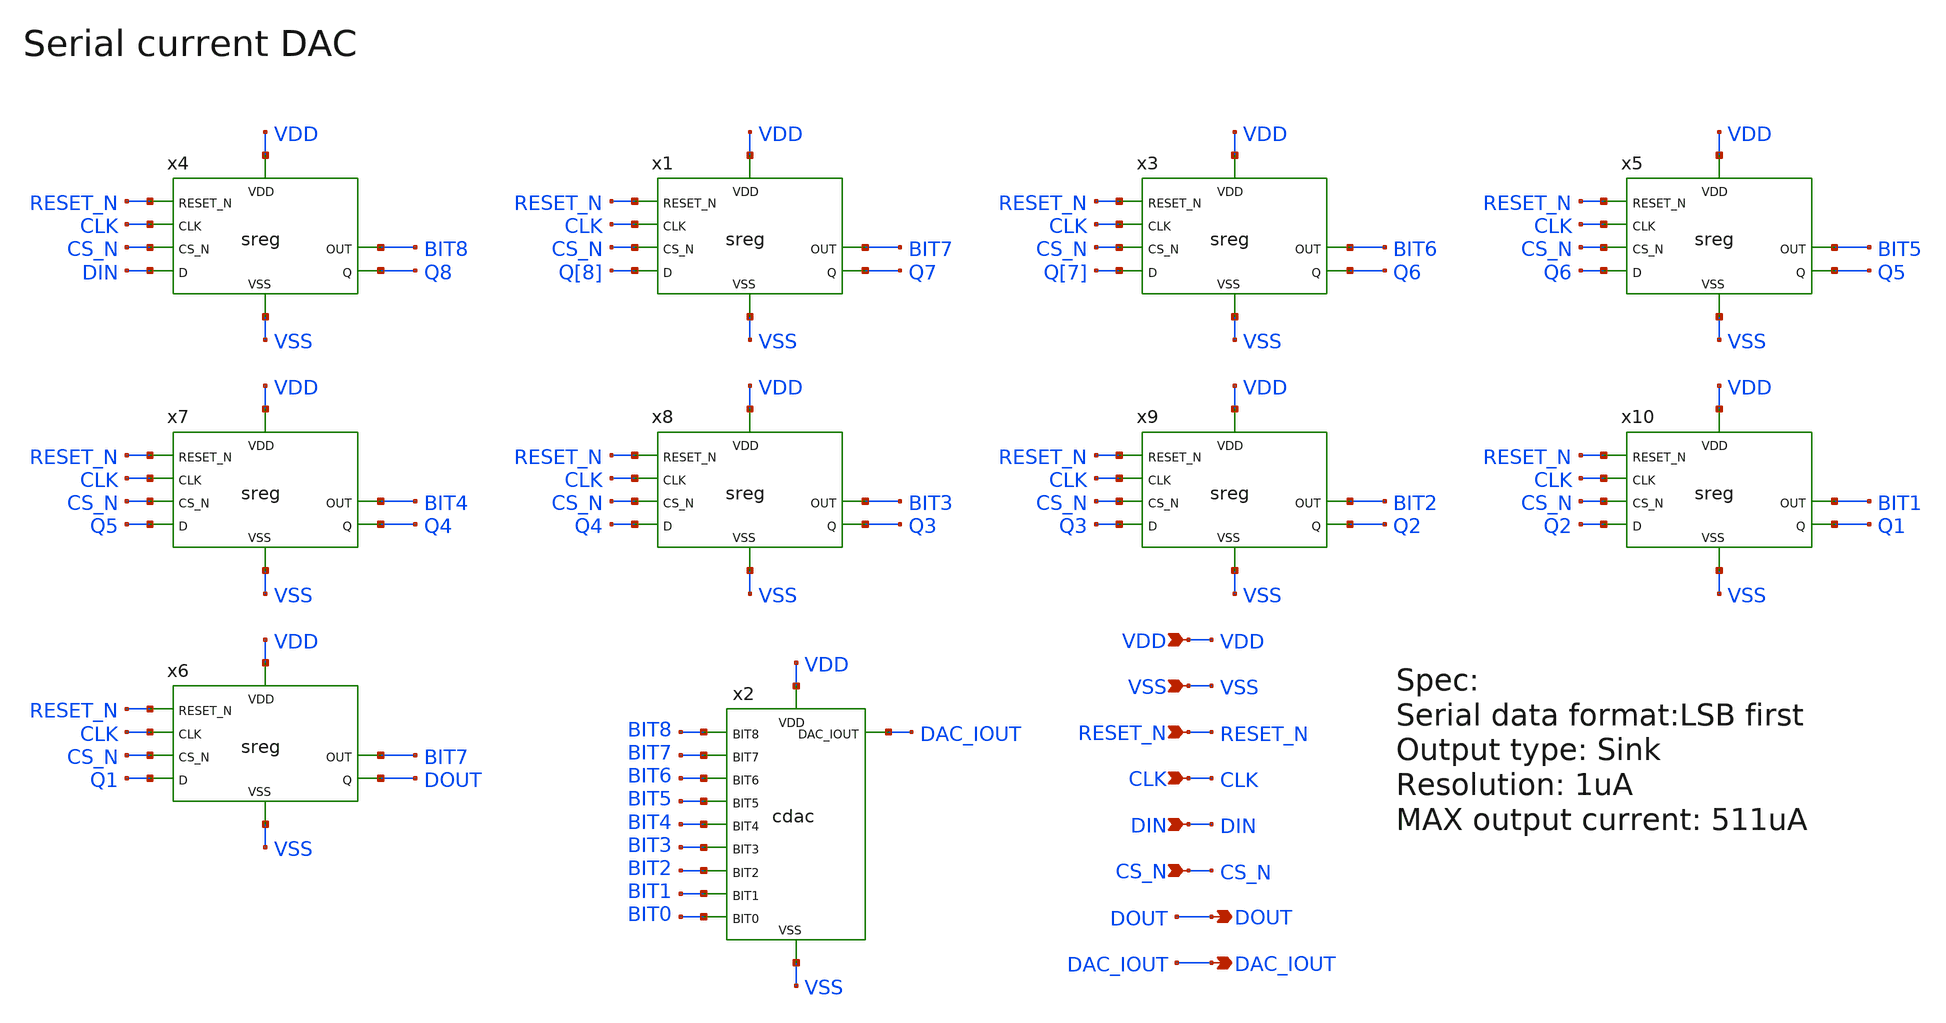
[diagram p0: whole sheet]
** sch_path: designs/libs/core_analog/scdac/scdac.sch
* Copyright 2022 GlobalFoundries PDK Authors
* Licensed under the Apache License, Version 2.0 (the "License");
* you may not use this file except in compliance with the License.
* You may obtain a copy of the License at
* https://www.apache.org/licenses/LICENSE-2.0
* Unless required by applicable law or agreed to in writing, software
* distributed under the License is distributed on an "AS IS" BASIS,
* WITHOUT WARRANTIES OR CONDITIONS OF ANY KIND, either express or implied.
* See the License for the specific language governing permissions and
* limitations under the License.
**.subckt scdac DAC_IOUT RESET_N CLK DIN CS_N VSS VDD DOUT
*.opin DAC_IOUT
*.ipin RESET_N
*.ipin CLK
*.ipin DIN
*.ipin CS_N
*.ipin VSS
*.ipin VDD
*.opin DOUT
x2 DAC_IOUT VSS VDD BIT8 BIT7 BIT6 BIT5 BIT4 BIT3 BIT2 BIT1 BIT0 cdac
x4 VDD VSS RESET_N CLK DIN CS_N Q8 BIT8 sreg
x1 VDD VSS RESET_N CLK Q[8] CS_N Q7 BIT7 sreg
x3 VDD VSS RESET_N CLK Q[7] CS_N Q6 BIT6 sreg
x5 VDD VSS RESET_N CLK Q6 CS_N Q5 BIT5 sreg
x6 VDD VSS RESET_N CLK Q1 CS_N DOUT BIT7 sreg
x7 VDD VSS RESET_N CLK Q5 CS_N Q4 BIT4 sreg
x8 VDD VSS RESET_N CLK Q4 CS_N Q3 BIT3 sreg
x9 VDD VSS RESET_N CLK Q3 CS_N Q2 BIT2 sreg
x10 VDD VSS RESET_N CLK Q2 CS_N Q1 BIT1 sreg
**.ends

* expanding   symbol:  libs/core_analog/scdac/cdac.sym # of pins=12
** sym_path: designs/libs/core_analog/scdac/cdac.sym
** sch_path: designs/libs/core_analog/scdac/cdac.sch
.subckt cdac DAC_IOUT VSS VDD BIT8 BIT7 BIT6 BIT5 BIT4 BIT3 BIT2 BIT1 BIT0
*.ipin BIT8
*.ipin BIT7
*.ipin BIT6
*.ipin BIT5
*.ipin BIT4
*.ipin BIT3
*.ipin BIT2
*.ipin BIT1
*.ipin BIT0
*.ipin VDD
*.ipin VSS
*.opin DAC_IOUT
XM8 64uA_REF 64uA_REF VSS VSS nfet_03v3 L=1u W=64u nf=1 ad='int((nf+1)/2) * W/nf * 0.18u' as='int((nf+2)/2) * W/nf * 0.18u'
+ pd='2*int((nf+1)/2) * (W/nf + 0.18u)' ps='2*int((nf+2)/2) * (W/nf + 0.18u)' nrd='0.18u / W' nrs='0.18u / W'
+ sa=0 sb=0 sd=0 m=1
XM11 net1 64uA_REF VSS VSS nfet_03v3 L=1u W=61.1u nf=1 ad='int((nf+1)/2) * W/nf * 0.18u' as='int((nf+2)/2) * W/nf * 0.18u'
+ pd='2*int((nf+1)/2) * (W/nf + 0.18u)' ps='2*int((nf+2)/2) * (W/nf + 0.18u)' nrd='0.18u / W' nrs='0.18u / W'
+ sa=0 sb=0 sd=0 m=1
XM13 DAC_IOUT BIT8 net1 VSS nfet_03v3 L=0.28u W=4u nf=1 ad='int((nf+1)/2) * W/nf * 0.18u' as='int((nf+2)/2) * W/nf * 0.18u'
+ pd='2*int((nf+1)/2) * (W/nf + 0.18u)' ps='2*int((nf+2)/2) * (W/nf + 0.18u)' nrd='0.18u / W' nrs='0.18u / W'
+ sa=0 sb=0 sd=0 m=1
XM15 net2 64uA_REF VSS VSS nfet_03v3 L=1u W=61.1u nf=1 ad='int((nf+1)/2) * W/nf * 0.18u' as='int((nf+2)/2) * W/nf * 0.18u'
+ pd='2*int((nf+1)/2) * (W/nf + 0.18u)' ps='2*int((nf+2)/2) * (W/nf + 0.18u)' nrd='0.18u / W' nrs='0.18u / W'
+ sa=0 sb=0 sd=0 m=1
XM16 DAC_IOUT BIT8 net2 VSS nfet_03v3 L=0.28u W=4u nf=1 ad='int((nf+1)/2) * W/nf * 0.18u' as='int((nf+2)/2) * W/nf * 0.18u'
+ pd='2*int((nf+1)/2) * (W/nf + 0.18u)' ps='2*int((nf+2)/2) * (W/nf + 0.18u)' nrd='0.18u / W' nrs='0.18u / W'
+ sa=0 sb=0 sd=0 m=1
XM18 net3 64uA_REF VSS VSS nfet_03v3 L=1u W=61.1u nf=1 ad='int((nf+1)/2) * W/nf * 0.18u' as='int((nf+2)/2) * W/nf * 0.18u'
+ pd='2*int((nf+1)/2) * (W/nf + 0.18u)' ps='2*int((nf+2)/2) * (W/nf + 0.18u)' nrd='0.18u / W' nrs='0.18u / W'
+ sa=0 sb=0 sd=0 m=1
XM19 DAC_IOUT BIT8 net3 VSS nfet_03v3 L=0.28u W=4u nf=1 ad='int((nf+1)/2) * W/nf * 0.18u' as='int((nf+2)/2) * W/nf * 0.18u'
+ pd='2*int((nf+1)/2) * (W/nf + 0.18u)' ps='2*int((nf+2)/2) * (W/nf + 0.18u)' nrd='0.18u / W' nrs='0.18u / W'
+ sa=0 sb=0 sd=0 m=1
XM21 net4 64uA_REF VSS VSS nfet_03v3 L=1u W=61.1u nf=1 ad='int((nf+1)/2) * W/nf * 0.18u' as='int((nf+2)/2) * W/nf * 0.18u'
+ pd='2*int((nf+1)/2) * (W/nf + 0.18u)' ps='2*int((nf+2)/2) * (W/nf + 0.18u)' nrd='0.18u / W' nrs='0.18u / W'
+ sa=0 sb=0 sd=0 m=1
XM22 DAC_IOUT BIT8 net4 VSS nfet_03v3 L=0.28u W=4u nf=1 ad='int((nf+1)/2) * W/nf * 0.18u' as='int((nf+2)/2) * W/nf * 0.18u'
+ pd='2*int((nf+1)/2) * (W/nf + 0.18u)' ps='2*int((nf+2)/2) * (W/nf + 0.18u)' nrd='0.18u / W' nrs='0.18u / W'
+ sa=0 sb=0 sd=0 m=1
XM24 net5 64uA_REF VSS VSS nfet_03v3 L=1u W=61.1u nf=1 ad='int((nf+1)/2) * W/nf * 0.18u' as='int((nf+2)/2) * W/nf * 0.18u'
+ pd='2*int((nf+1)/2) * (W/nf + 0.18u)' ps='2*int((nf+2)/2) * (W/nf + 0.18u)' nrd='0.18u / W' nrs='0.18u / W'
+ sa=0 sb=0 sd=0 m=1
XM25 DAC_IOUT BIT7 net5 VSS nfet_03v3 L=0.28u W=4u nf=1 ad='int((nf+1)/2) * W/nf * 0.18u' as='int((nf+2)/2) * W/nf * 0.18u'
+ pd='2*int((nf+1)/2) * (W/nf + 0.18u)' ps='2*int((nf+2)/2) * (W/nf + 0.18u)' nrd='0.18u / W' nrs='0.18u / W'
+ sa=0 sb=0 sd=0 m=1
XM27 net6 64uA_REF VSS VSS nfet_03v3 L=1u W=61.1u nf=1 ad='int((nf+1)/2) * W/nf * 0.18u' as='int((nf+2)/2) * W/nf * 0.18u'
+ pd='2*int((nf+1)/2) * (W/nf + 0.18u)' ps='2*int((nf+2)/2) * (W/nf + 0.18u)' nrd='0.18u / W' nrs='0.18u / W'
+ sa=0 sb=0 sd=0 m=1
XM28 DAC_IOUT BIT7 net6 VSS nfet_03v3 L=0.28u W=4u nf=1 ad='int((nf+1)/2) * W/nf * 0.18u' as='int((nf+2)/2) * W/nf * 0.18u'
+ pd='2*int((nf+1)/2) * (W/nf + 0.18u)' ps='2*int((nf+2)/2) * (W/nf + 0.18u)' nrd='0.18u / W' nrs='0.18u / W'
+ sa=0 sb=0 sd=0 m=1
XM30 net7 64uA_REF VSS VSS nfet_03v3 L=1u W=61.1u nf=1 ad='int((nf+1)/2) * W/nf * 0.18u' as='int((nf+2)/2) * W/nf * 0.18u'
+ pd='2*int((nf+1)/2) * (W/nf + 0.18u)' ps='2*int((nf+2)/2) * (W/nf + 0.18u)' nrd='0.18u / W' nrs='0.18u / W'
+ sa=0 sb=0 sd=0 m=1
XM31 DAC_IOUT BIT6 net7 VSS nfet_03v3 L=0.28u W=4u nf=8 ad='int((nf+1)/2) * W/nf * 0.18u' as='int((nf+2)/2) * W/nf * 0.18u'
+ pd='2*int((nf+1)/2) * (W/nf + 0.18u)' ps='2*int((nf+2)/2) * (W/nf + 0.18u)' nrd='0.18u / W' nrs='0.18u / W'
+ sa=0 sb=0 sd=0 m=1
XM1 net8 64uA_REF VSS VSS nfet_03v3 L=1u W=7.62u nf=1 ad='int((nf+1)/2) * W/nf * 0.18u' as='int((nf+2)/2) * W/nf * 0.18u'
+ pd='2*int((nf+1)/2) * (W/nf + 0.18u)' ps='2*int((nf+2)/2) * (W/nf + 0.18u)' nrd='0.18u / W' nrs='0.18u / W'
+ sa=0 sb=0 sd=0 m=1
XM2 DAC_IOUT BIT5 net8 VSS nfet_03v3 L=0.28u W=4u nf=1 ad='int((nf+1)/2) * W/nf * 0.18u' as='int((nf+2)/2) * W/nf * 0.18u'
+ pd='2*int((nf+1)/2) * (W/nf + 0.18u)' ps='2*int((nf+2)/2) * (W/nf + 0.18u)' nrd='0.18u / W' nrs='0.18u / W'
+ sa=0 sb=0 sd=0 m=1
XM3 net9 64uA_REF VSS VSS nfet_03v3 L=1u W=7.62u nf=1 ad='int((nf+1)/2) * W/nf * 0.18u' as='int((nf+2)/2) * W/nf * 0.18u'
+ pd='2*int((nf+1)/2) * (W/nf + 0.18u)' ps='2*int((nf+2)/2) * (W/nf + 0.18u)' nrd='0.18u / W' nrs='0.18u / W'
+ sa=0 sb=0 sd=0 m=1
XM4 DAC_IOUT BIT5 net9 VSS nfet_03v3 L=0.28u W=4u nf=1 ad='int((nf+1)/2) * W/nf * 0.18u' as='int((nf+2)/2) * W/nf * 0.18u'
+ pd='2*int((nf+1)/2) * (W/nf + 0.18u)' ps='2*int((nf+2)/2) * (W/nf + 0.18u)' nrd='0.18u / W' nrs='0.18u / W'
+ sa=0 sb=0 sd=0 m=1
XM5 net10 64uA_REF VSS VSS nfet_03v3 L=1u W=7.62u nf=1 ad='int((nf+1)/2) * W/nf * 0.18u' as='int((nf+2)/2) * W/nf * 0.18u'
+ pd='2*int((nf+1)/2) * (W/nf + 0.18u)' ps='2*int((nf+2)/2) * (W/nf + 0.18u)' nrd='0.18u / W' nrs='0.18u / W'
+ sa=0 sb=0 sd=0 m=1
XM6 DAC_IOUT BIT5 net10 VSS nfet_03v3 L=0.28u W=4u nf=1 ad='int((nf+1)/2) * W/nf * 0.18u' as='int((nf+2)/2) * W/nf * 0.18u'
+ pd='2*int((nf+1)/2) * (W/nf + 0.18u)' ps='2*int((nf+2)/2) * (W/nf + 0.18u)' nrd='0.18u / W' nrs='0.18u / W'
+ sa=0 sb=0 sd=0 m=1
XM7 net11 64uA_REF VSS VSS nfet_03v3 L=1u W=7.62u nf=1 ad='int((nf+1)/2) * W/nf * 0.18u' as='int((nf+2)/2) * W/nf * 0.18u'
+ pd='2*int((nf+1)/2) * (W/nf + 0.18u)' ps='2*int((nf+2)/2) * (W/nf + 0.18u)' nrd='0.18u / W' nrs='0.18u / W'
+ sa=0 sb=0 sd=0 m=1
XM9 DAC_IOUT BIT5 net11 VSS nfet_03v3 L=0.28u W=4u nf=1 ad='int((nf+1)/2) * W/nf * 0.18u' as='int((nf+2)/2) * W/nf * 0.18u'
+ pd='2*int((nf+1)/2) * (W/nf + 0.18u)' ps='2*int((nf+2)/2) * (W/nf + 0.18u)' nrd='0.18u / W' nrs='0.18u / W'
+ sa=0 sb=0 sd=0 m=1
XM10 net12 64uA_REF VSS VSS nfet_03v3 L=1u W=7.62u nf=1 ad='int((nf+1)/2) * W/nf * 0.18u' as='int((nf+2)/2) * W/nf * 0.18u'
+ pd='2*int((nf+1)/2) * (W/nf + 0.18u)' ps='2*int((nf+2)/2) * (W/nf + 0.18u)' nrd='0.18u / W' nrs='0.18u / W'
+ sa=0 sb=0 sd=0 m=1
XM12 DAC_IOUT BIT4 net12 VSS nfet_03v3 L=0.28u W=4u nf=1 ad='int((nf+1)/2) * W/nf * 0.18u' as='int((nf+2)/2) * W/nf * 0.18u'
+ pd='2*int((nf+1)/2) * (W/nf + 0.18u)' ps='2*int((nf+2)/2) * (W/nf + 0.18u)' nrd='0.18u / W' nrs='0.18u / W'
+ sa=0 sb=0 sd=0 m=1
XM14 net13 64uA_REF VSS VSS nfet_03v3 L=1u W=7.62u nf=1 ad='int((nf+1)/2) * W/nf * 0.18u' as='int((nf+2)/2) * W/nf * 0.18u'
+ pd='2*int((nf+1)/2) * (W/nf + 0.18u)' ps='2*int((nf+2)/2) * (W/nf + 0.18u)' nrd='0.18u / W' nrs='0.18u / W'
+ sa=0 sb=0 sd=0 m=1
XM17 DAC_IOUT BIT4 net13 VSS nfet_03v3 L=0.28u W=4u nf=1 ad='int((nf+1)/2) * W/nf * 0.18u' as='int((nf+2)/2) * W/nf * 0.18u'
+ pd='2*int((nf+1)/2) * (W/nf + 0.18u)' ps='2*int((nf+2)/2) * (W/nf + 0.18u)' nrd='0.18u / W' nrs='0.18u / W'
+ sa=0 sb=0 sd=0 m=1
XM20 net14 64uA_REF VSS VSS nfet_03v3 L=1u W=7.62u nf=1 ad='int((nf+1)/2) * W/nf * 0.18u' as='int((nf+2)/2) * W/nf * 0.18u'
+ pd='2*int((nf+1)/2) * (W/nf + 0.18u)' ps='2*int((nf+2)/2) * (W/nf + 0.18u)' nrd='0.18u / W' nrs='0.18u / W'
+ sa=0 sb=0 sd=0 m=1
XM23 DAC_IOUT BIT3 net14 VSS nfet_03v3 L=0.28u W=4u nf=1 ad='int((nf+1)/2) * W/nf * 0.18u' as='int((nf+2)/2) * W/nf * 0.18u'
+ pd='2*int((nf+1)/2) * (W/nf + 0.18u)' ps='2*int((nf+2)/2) * (W/nf + 0.18u)' nrd='0.18u / W' nrs='0.18u / W'
+ sa=0 sb=0 sd=0 m=1
XM26 net15 64uA_REF VSS VSS nfet_03v3 L=1u W=1.01u nf=1 ad='int((nf+1)/2) * W/nf * 0.18u' as='int((nf+2)/2) * W/nf * 0.18u'
+ pd='2*int((nf+1)/2) * (W/nf + 0.18u)' ps='2*int((nf+2)/2) * (W/nf + 0.18u)' nrd='0.18u / W' nrs='0.18u / W'
+ sa=0 sb=0 sd=0 m=1
XM29 DAC_IOUT BIT2 net15 VSS nfet_03v3 L=0.28u W=4u nf=1 ad='int((nf+1)/2) * W/nf * 0.18u' as='int((nf+2)/2) * W/nf * 0.18u'
+ pd='2*int((nf+1)/2) * (W/nf + 0.18u)' ps='2*int((nf+2)/2) * (W/nf + 0.18u)' nrd='0.18u / W' nrs='0.18u / W'
+ sa=0 sb=0 sd=0 m=1
XM32 net16 64uA_REF VSS VSS nfet_03v3 L=1u W=1.01u nf=1 ad='int((nf+1)/2) * W/nf * 0.18u' as='int((nf+2)/2) * W/nf * 0.18u'
+ pd='2*int((nf+1)/2) * (W/nf + 0.18u)' ps='2*int((nf+2)/2) * (W/nf + 0.18u)' nrd='0.18u / W' nrs='0.18u / W'
+ sa=0 sb=0 sd=0 m=1
XM35 DAC_IOUT BIT2 net16 VSS nfet_03v3 L=0.28u W=4u nf=1 ad='int((nf+1)/2) * W/nf * 0.18u' as='int((nf+2)/2) * W/nf * 0.18u'
+ pd='2*int((nf+1)/2) * (W/nf + 0.18u)' ps='2*int((nf+2)/2) * (W/nf + 0.18u)' nrd='0.18u / W' nrs='0.18u / W'
+ sa=0 sb=0 sd=0 m=1
XM36 net17 64uA_REF VSS VSS nfet_03v3 L=1u W=1.01u nf=1 ad='int((nf+1)/2) * W/nf * 0.18u' as='int((nf+2)/2) * W/nf * 0.18u'
+ pd='2*int((nf+1)/2) * (W/nf + 0.18u)' ps='2*int((nf+2)/2) * (W/nf + 0.18u)' nrd='0.18u / W' nrs='0.18u / W'
+ sa=0 sb=0 sd=0 m=1
XM37 DAC_IOUT BIT2 net17 VSS nfet_03v3 L=0.28u W=4u nf=1 ad='int((nf+1)/2) * W/nf * 0.18u' as='int((nf+2)/2) * W/nf * 0.18u'
+ pd='2*int((nf+1)/2) * (W/nf + 0.18u)' ps='2*int((nf+2)/2) * (W/nf + 0.18u)' nrd='0.18u / W' nrs='0.18u / W'
+ sa=0 sb=0 sd=0 m=1
XM38 net18 64uA_REF VSS VSS nfet_03v3 L=1u W=1.01u nf=1 ad='int((nf+1)/2) * W/nf * 0.18u' as='int((nf+2)/2) * W/nf * 0.18u'
+ pd='2*int((nf+1)/2) * (W/nf + 0.18u)' ps='2*int((nf+2)/2) * (W/nf + 0.18u)' nrd='0.18u / W' nrs='0.18u / W'
+ sa=0 sb=0 sd=0 m=1
XM39 DAC_IOUT BIT2 net18 VSS nfet_03v3 L=0.28u W=4u nf=1 ad='int((nf+1)/2) * W/nf * 0.18u' as='int((nf+2)/2) * W/nf * 0.18u'
+ pd='2*int((nf+1)/2) * (W/nf + 0.18u)' ps='2*int((nf+2)/2) * (W/nf + 0.18u)' nrd='0.18u / W' nrs='0.18u / W'
+ sa=0 sb=0 sd=0 m=1
XM40 net19 64uA_REF VSS VSS nfet_03v3 L=1u W=1.01u nf=1 ad='int((nf+1)/2) * W/nf * 0.18u' as='int((nf+2)/2) * W/nf * 0.18u'
+ pd='2*int((nf+1)/2) * (W/nf + 0.18u)' ps='2*int((nf+2)/2) * (W/nf + 0.18u)' nrd='0.18u / W' nrs='0.18u / W'
+ sa=0 sb=0 sd=0 m=1
XM41 DAC_IOUT BIT1 net19 VSS nfet_03v3 L=0.28u W=4u nf=1 ad='int((nf+1)/2) * W/nf * 0.18u' as='int((nf+2)/2) * W/nf * 0.18u'
+ pd='2*int((nf+1)/2) * (W/nf + 0.18u)' ps='2*int((nf+2)/2) * (W/nf + 0.18u)' nrd='0.18u / W' nrs='0.18u / W'
+ sa=0 sb=0 sd=0 m=1
XM42 net20 64uA_REF VSS VSS nfet_03v3 L=1u W=1.01u nf=1 ad='int((nf+1)/2) * W/nf * 0.18u' as='int((nf+2)/2) * W/nf * 0.18u'
+ pd='2*int((nf+1)/2) * (W/nf + 0.18u)' ps='2*int((nf+2)/2) * (W/nf + 0.18u)' nrd='0.18u / W' nrs='0.18u / W'
+ sa=0 sb=0 sd=0 m=1
XM43 DAC_IOUT BIT1 net20 VSS nfet_03v3 L=0.28u W=4u nf=1 ad='int((nf+1)/2) * W/nf * 0.18u' as='int((nf+2)/2) * W/nf * 0.18u'
+ pd='2*int((nf+1)/2) * (W/nf + 0.18u)' ps='2*int((nf+2)/2) * (W/nf + 0.18u)' nrd='0.18u / W' nrs='0.18u / W'
+ sa=0 sb=0 sd=0 m=1
XM44 net21 64uA_REF VSS VSS nfet_03v3 L=1u W=1.01u nf=1 ad='int((nf+1)/2) * W/nf * 0.18u' as='int((nf+2)/2) * W/nf * 0.18u'
+ pd='2*int((nf+1)/2) * (W/nf + 0.18u)' ps='2*int((nf+2)/2) * (W/nf + 0.18u)' nrd='0.18u / W' nrs='0.18u / W'
+ sa=0 sb=0 sd=0 m=1
XM45 DAC_IOUT BIT0 net21 VSS nfet_03v3 L=0.28u W=4u nf=1 ad='int((nf+1)/2) * W/nf * 0.18u' as='int((nf+2)/2) * W/nf * 0.18u'
+ pd='2*int((nf+1)/2) * (W/nf + 0.18u)' ps='2*int((nf+2)/2) * (W/nf + 0.18u)' nrd='0.18u / W' nrs='0.18u / W'
+ sa=0 sb=0 sd=0 m=1
x1 VDD VSS 64uA_REF bmr
.ends


* expanding   symbol:  libs/core_analog/sreg/sreg.sym # of pins=8
** sym_path: designs/libs/core_analog/sreg/sreg.sym
** sch_path: designs/libs/core_analog/sreg/sreg.sch
.subckt sreg VDD VSS RESET_N CLK D CS_N Q OUT
*.ipin RESET_N
*.ipin CLK
*.ipin D
*.ipin CS_N
*.ipin VSS
*.ipin VDD
*.opin Q
*.opin OUT
x11 net1 RESET_N CLK Q VDD VDD VSS VSS gf180mcu_fd_sc_mcu7t5v0__dffrnq_1
x15 net2 RESET_N CS_N OUT VDD VDD VSS VSS gf180mcu_fd_sc_mcu7t5v0__dffrnq_1
x1 D Q CS_N net1 VDD VDD VSS VSS gf180mcu_fd_sc_mcu7t5v0__mux2_2
x2 Q OUT CS_N net2 VDD VDD VSS VSS gf180mcu_fd_sc_mcu7t5v0__mux2_2
.ends


* expanding   symbol:  libs/core_analog/bmr/bmr.sym # of pins=3
** sym_path: designs/libs/core_analog/bmr/bmr.sym
** sch_path: designs/libs/core_analog/bmr/bmr.sch
.subckt bmr VDD VSS 64uA_OUT
*.ipin VDD
*.ipin VSS
*.opin 64uA_OUT
XM3 net2 net1 net3 VSS nfet_03v3 L=1u W=10u nf=1 ad='int((nf+1)/2) * W/nf * 0.18u' as='int((nf+2)/2) * W/nf * 0.18u'
+ pd='2*int((nf+1)/2) * (W/nf + 0.18u)' ps='2*int((nf+2)/2) * (W/nf + 0.18u)' nrd='0.18u / W' nrs='0.18u / W'
+ sa=0 sb=0 sd=0 m=1
XM5 net3 net2 VDD VDD pfet_03v3 L=3u W=15u nf=1 ad='int((nf+1)/2) * W/nf * 0.18u' as='int((nf+2)/2) * W/nf * 0.18u'
+ pd='2*int((nf+1)/2) * (W/nf + 0.18u)' ps='2*int((nf+2)/2) * (W/nf + 0.18u)' nrd='0.18u / W' nrs='0.18u / W'
+ sa=0 sb=0 sd=0 m=1
XM6 net1 net1 VDD VDD pfet_03v3 L=4u W=4u nf=1 ad='int((nf+1)/2) * W/nf * 0.18u' as='int((nf+2)/2) * W/nf * 0.18u'
+ pd='2*int((nf+1)/2) * (W/nf + 0.18u)' ps='2*int((nf+2)/2) * (W/nf + 0.18u)' nrd='0.18u / W' nrs='0.18u / W'
+ sa=0 sb=0 sd=0 m=1
XM9 net2 net3 net4 VSS nfet_03v3 L=3u W=10u nf=1 ad='int((nf+1)/2) * W/nf * 0.18u' as='int((nf+2)/2) * W/nf * 0.18u'
+ pd='2*int((nf+1)/2) * (W/nf + 0.18u)' ps='2*int((nf+2)/2) * (W/nf + 0.18u)' nrd='0.18u / W' nrs='0.18u / W'
+ sa=0 sb=0 sd=0 m=1
XM12 net2 net2 VDD VDD pfet_03v3 L=3u W=15u nf=1 ad='int((nf+1)/2) * W/nf * 0.18u' as='int((nf+2)/2) * W/nf * 0.18u'
+ pd='2*int((nf+1)/2) * (W/nf + 0.18u)' ps='2*int((nf+2)/2) * (W/nf + 0.18u)' nrd='0.18u / W' nrs='0.18u / W'
+ sa=0 sb=0 sd=0 m=1
XM1 net1 net3 VSS VSS nfet_03v3 L=3u W=10u nf=1 ad='int((nf+1)/2) * W/nf * 0.18u' as='int((nf+2)/2) * W/nf * 0.18u'
+ pd='2*int((nf+1)/2) * (W/nf + 0.18u)' ps='2*int((nf+2)/2) * (W/nf + 0.18u)' nrd='0.18u / W' nrs='0.18u / W'
+ sa=0 sb=0 sd=0 m=1
XM2 net3 net3 VSS VSS nfet_03v3 L=3u W=5u nf=1 ad='int((nf+1)/2) * W/nf * 0.18u' as='int((nf+2)/2) * W/nf * 0.18u'
+ pd='2*int((nf+1)/2) * (W/nf + 0.18u)' ps='2*int((nf+2)/2) * (W/nf + 0.18u)' nrd='0.18u / W' nrs='0.18u / W'
+ sa=0 sb=0 sd=0 m=1
XM4 64uA_OUT net2 VDD VDD pfet_03v3 L=3u W=15u nf=1 ad='int((nf+1)/2) * W/nf * 0.18u' as='int((nf+2)/2) * W/nf * 0.18u'
+ pd='2*int((nf+1)/2) * (W/nf + 0.18u)' ps='2*int((nf+2)/2) * (W/nf + 0.18u)' nrd='0.18u / W' nrs='0.18u / W'
+ sa=0 sb=0 sd=0 m=1
XR2 VSS net4 VDD ppolyf_u_1k r_width=1e-6 r_length=2.61e-6 m=1
.ends

.end
